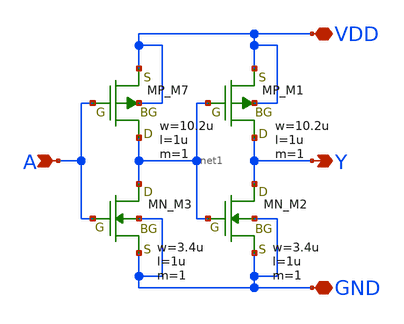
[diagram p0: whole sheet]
** sch_path: libs.tech/xschem/TR-1um_5_stdcell/BUF_X1.sch
**.subckt BUF_X1 A Y VDD GND
*.ipin A
*.opin Y
*.iopin VDD
*.iopin GND
XM7 net1 A VDD VDD PMOS w=10.2u l=1u nrd=0 nrs=0 m=1
XM1 Y net1 VDD VDD PMOS w=10.2u l=1u nrd=0 nrs=0 m=1
XM3 net1 A GND GND NMOS w=3.4u l=1u nrd=0 nrs=0 m=1
XM2 Y net1 GND GND NMOS w=3.4u l=1u nrd=0 nrs=0 m=1
**.ends
.end
